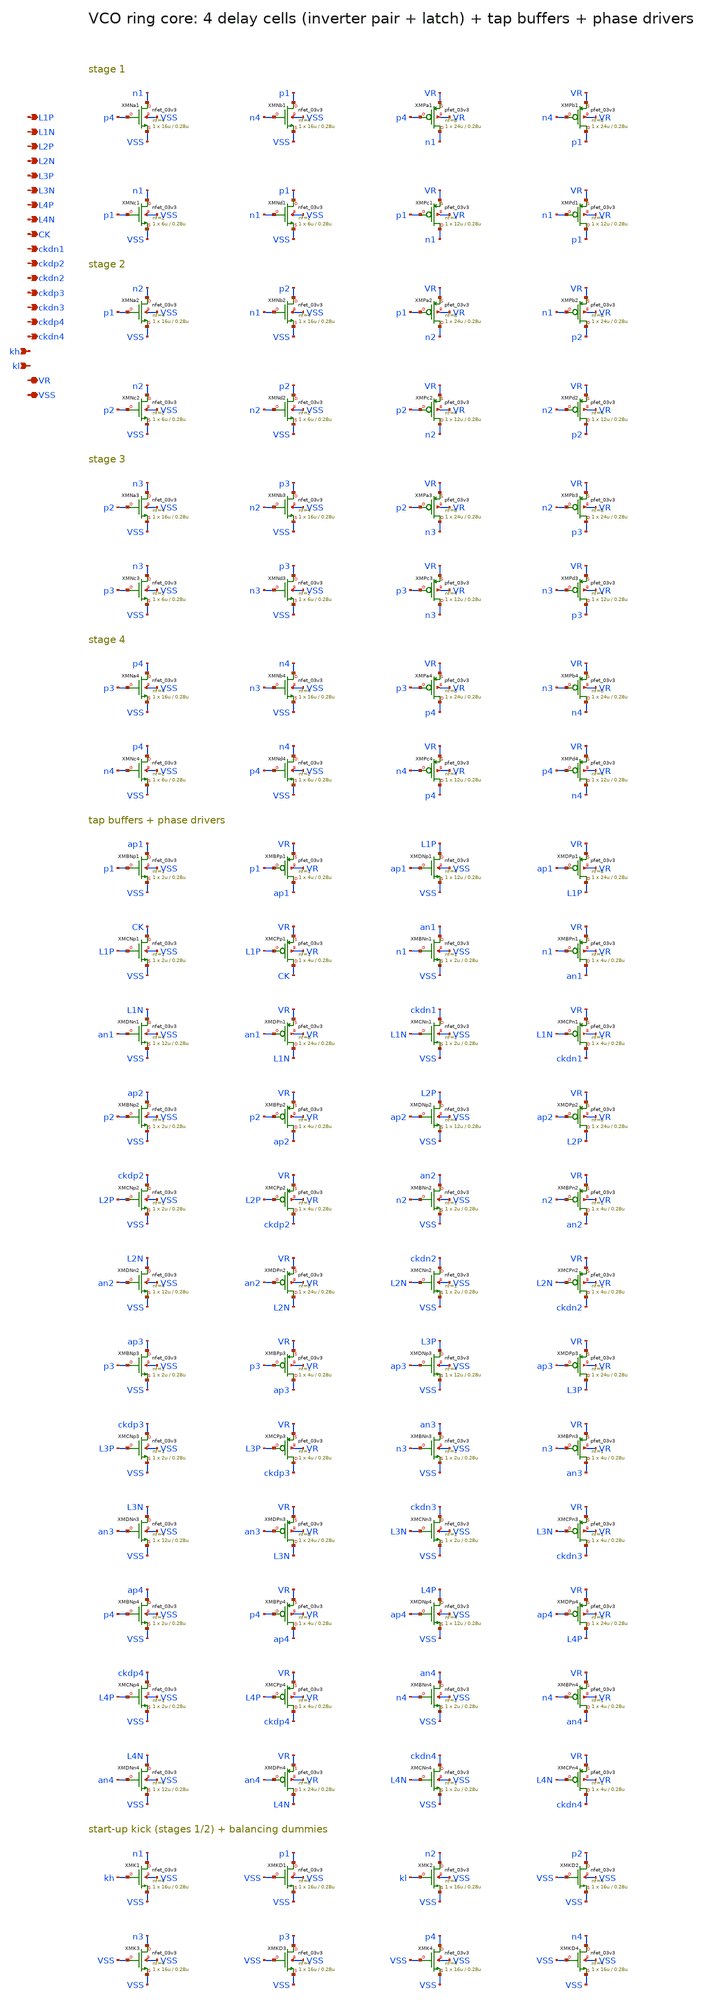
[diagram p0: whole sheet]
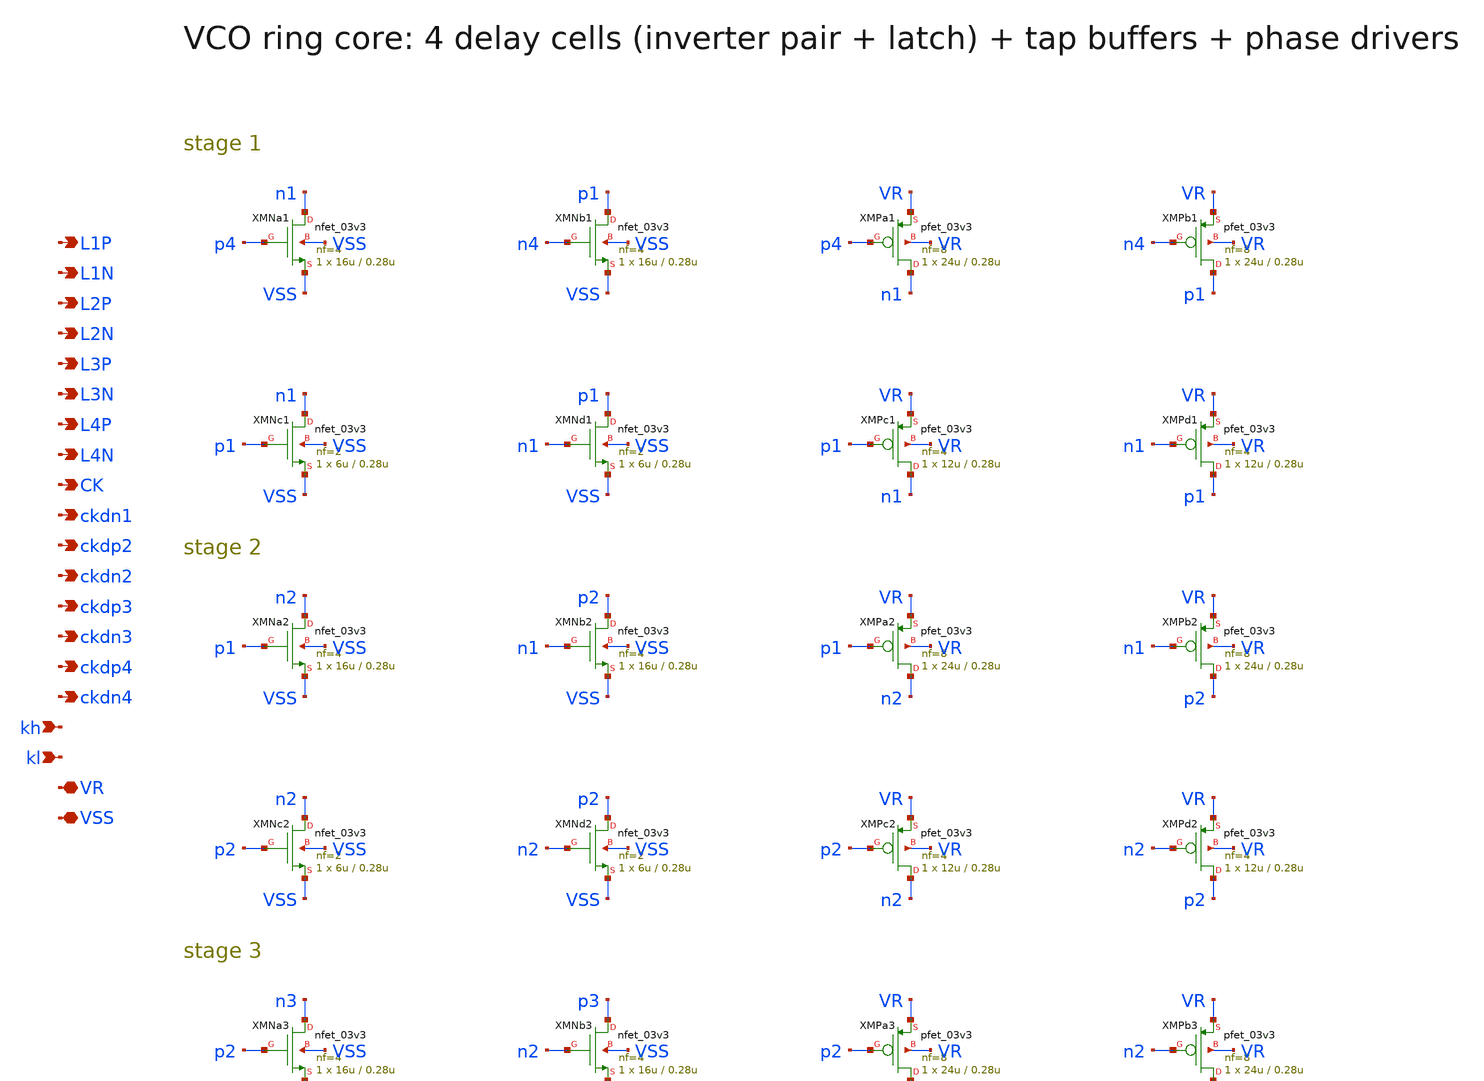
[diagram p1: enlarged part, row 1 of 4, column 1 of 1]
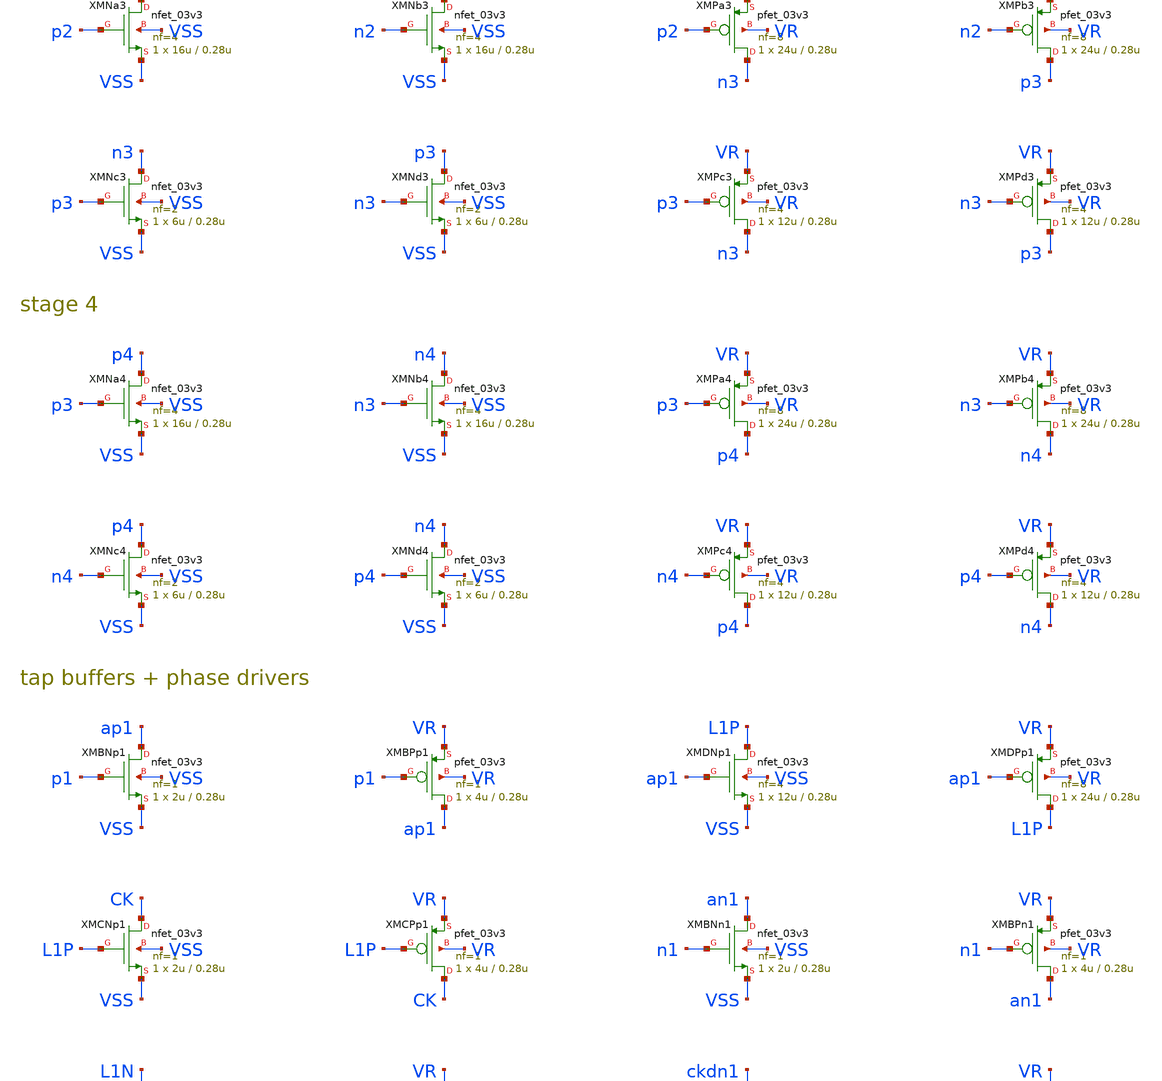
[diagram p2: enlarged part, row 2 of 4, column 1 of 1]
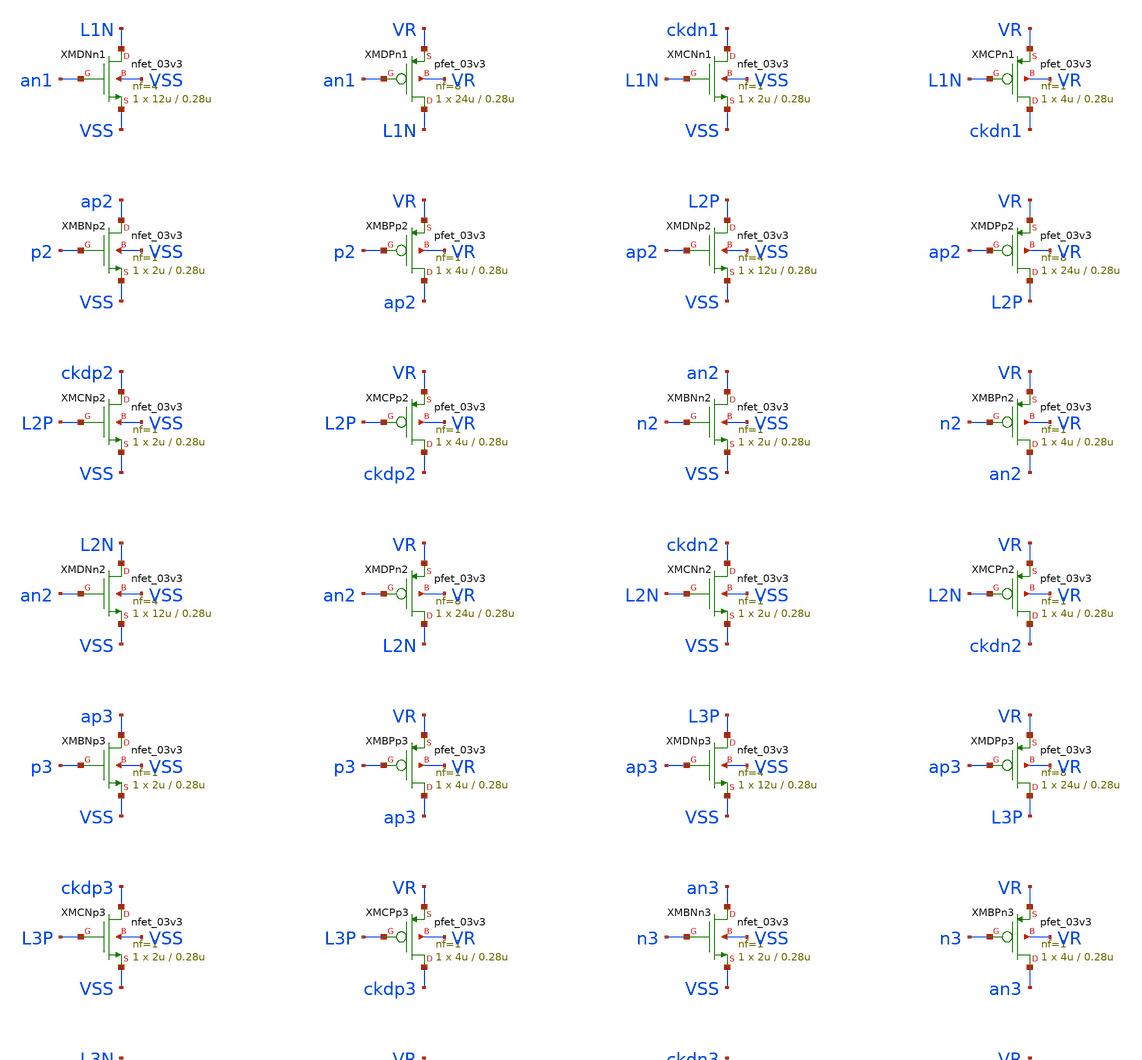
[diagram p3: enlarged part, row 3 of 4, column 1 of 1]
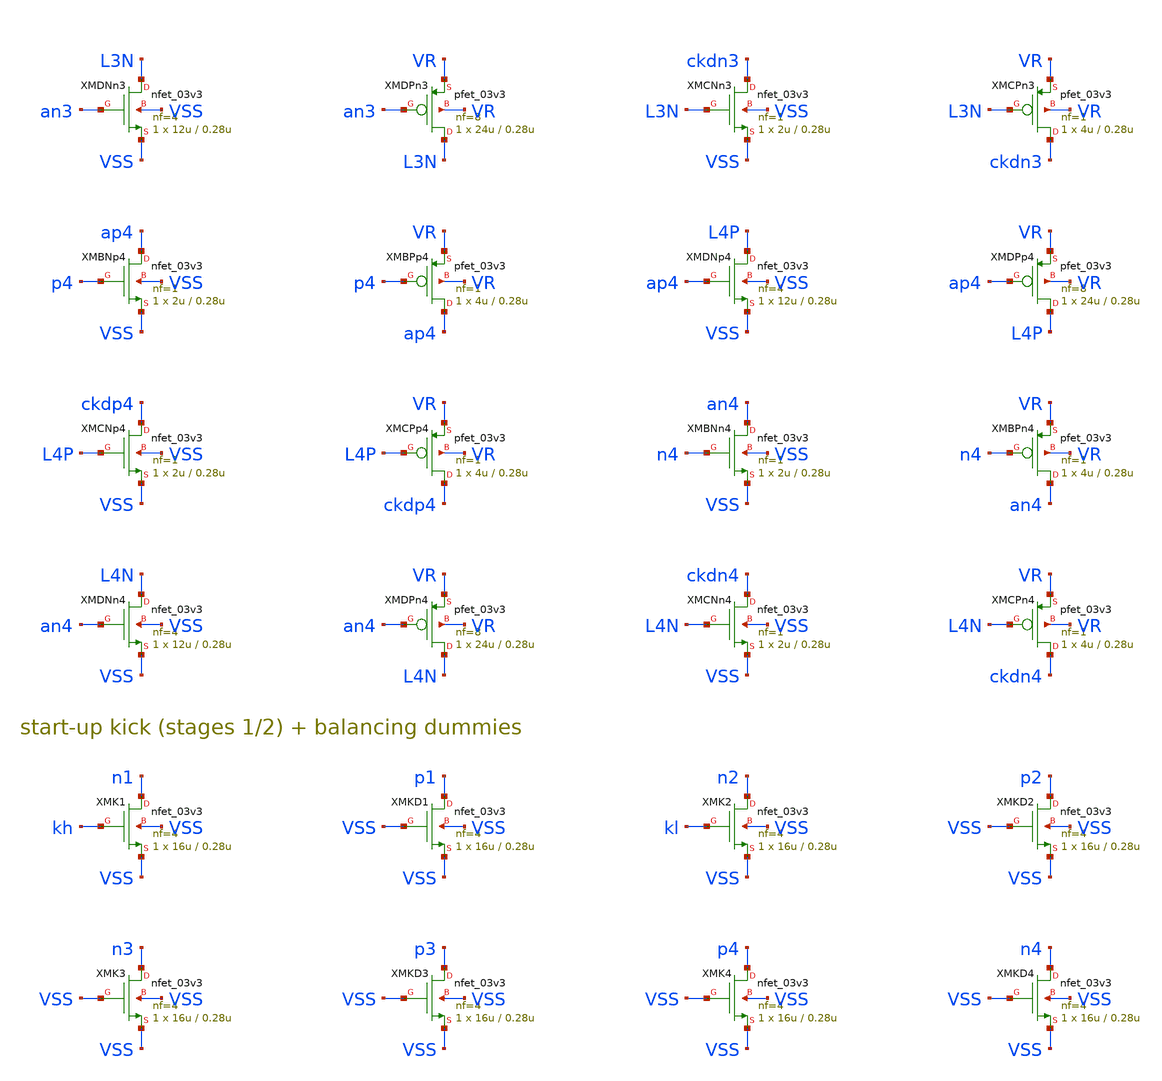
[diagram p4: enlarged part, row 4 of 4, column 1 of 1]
** sch_path: v1_claude/xschem/vco_core.sch
**.subckt vco_core L1P L1N L2P L2N L3P L3N L4P L4N CK ckdn1 ckdp2 ckdn2 ckdp3 ckdn3 ckdp4 ckdn4 kh
*+ kl VR VSS
*.opin L1P
*.opin L1N
*.opin L2P
*.opin L2N
*.opin L3P
*.opin L3N
*.opin L4P
*.opin L4N
*.opin CK
*.opin ckdn1
*.opin ckdp2
*.opin ckdn2
*.opin ckdp3
*.opin ckdn3
*.opin ckdp4
*.opin ckdn4
*.ipin kh
*.ipin kl
*.iopin VR
*.iopin VSS
XMNa1 n1 p4 VSS VSS nfet_03v3 L=0.28u W=16u nf=4 ad='int((nf+1)/2) * W/nf * 0.18u' as='int((nf+2)/2) * W/nf * 0.18u'
+ pd='2*int((nf+1)/2) * (W/nf + 0.18u)' ps='2*int((nf+2)/2) * (W/nf + 0.18u)' nrd='0.18u / W' nrs='0.18u / W'
+ sa=0 sb=0 sd=0 m=1
XMNb1 p1 n4 VSS VSS nfet_03v3 L=0.28u W=16u nf=4 ad='int((nf+1)/2) * W/nf * 0.18u' as='int((nf+2)/2) * W/nf * 0.18u'
+ pd='2*int((nf+1)/2) * (W/nf + 0.18u)' ps='2*int((nf+2)/2) * (W/nf + 0.18u)' nrd='0.18u / W' nrs='0.18u / W'
+ sa=0 sb=0 sd=0 m=1
XMPa1 n1 p4 VR VR pfet_03v3 L=0.28u W=24u nf=8 ad='int((nf+1)/2) * W/nf * 0.18u' as='int((nf+2)/2) * W/nf * 0.18u'
+ pd='2*int((nf+1)/2) * (W/nf + 0.18u)' ps='2*int((nf+2)/2) * (W/nf + 0.18u)' nrd='0.18u / W' nrs='0.18u / W'
+ sa=0 sb=0 sd=0 m=1
XMPb1 p1 n4 VR VR pfet_03v3 L=0.28u W=24u nf=8 ad='int((nf+1)/2) * W/nf * 0.18u' as='int((nf+2)/2) * W/nf * 0.18u'
+ pd='2*int((nf+1)/2) * (W/nf + 0.18u)' ps='2*int((nf+2)/2) * (W/nf + 0.18u)' nrd='0.18u / W' nrs='0.18u / W'
+ sa=0 sb=0 sd=0 m=1
XMNc1 n1 p1 VSS VSS nfet_03v3 L=0.28u W=6u nf=2 ad='int((nf+1)/2) * W/nf * 0.18u' as='int((nf+2)/2) * W/nf * 0.18u'
+ pd='2*int((nf+1)/2) * (W/nf + 0.18u)' ps='2*int((nf+2)/2) * (W/nf + 0.18u)' nrd='0.18u / W' nrs='0.18u / W'
+ sa=0 sb=0 sd=0 m=1
XMNd1 p1 n1 VSS VSS nfet_03v3 L=0.28u W=6u nf=2 ad='int((nf+1)/2) * W/nf * 0.18u' as='int((nf+2)/2) * W/nf * 0.18u'
+ pd='2*int((nf+1)/2) * (W/nf + 0.18u)' ps='2*int((nf+2)/2) * (W/nf + 0.18u)' nrd='0.18u / W' nrs='0.18u / W'
+ sa=0 sb=0 sd=0 m=1
XMPc1 n1 p1 VR VR pfet_03v3 L=0.28u W=12u nf=4 ad='int((nf+1)/2) * W/nf * 0.18u' as='int((nf+2)/2) * W/nf * 0.18u'
+ pd='2*int((nf+1)/2) * (W/nf + 0.18u)' ps='2*int((nf+2)/2) * (W/nf + 0.18u)' nrd='0.18u / W' nrs='0.18u / W'
+ sa=0 sb=0 sd=0 m=1
XMPd1 p1 n1 VR VR pfet_03v3 L=0.28u W=12u nf=4 ad='int((nf+1)/2) * W/nf * 0.18u' as='int((nf+2)/2) * W/nf * 0.18u'
+ pd='2*int((nf+1)/2) * (W/nf + 0.18u)' ps='2*int((nf+2)/2) * (W/nf + 0.18u)' nrd='0.18u / W' nrs='0.18u / W'
+ sa=0 sb=0 sd=0 m=1
XMNa2 n2 p1 VSS VSS nfet_03v3 L=0.28u W=16u nf=4 ad='int((nf+1)/2) * W/nf * 0.18u' as='int((nf+2)/2) * W/nf * 0.18u'
+ pd='2*int((nf+1)/2) * (W/nf + 0.18u)' ps='2*int((nf+2)/2) * (W/nf + 0.18u)' nrd='0.18u / W' nrs='0.18u / W'
+ sa=0 sb=0 sd=0 m=1
XMNb2 p2 n1 VSS VSS nfet_03v3 L=0.28u W=16u nf=4 ad='int((nf+1)/2) * W/nf * 0.18u' as='int((nf+2)/2) * W/nf * 0.18u'
+ pd='2*int((nf+1)/2) * (W/nf + 0.18u)' ps='2*int((nf+2)/2) * (W/nf + 0.18u)' nrd='0.18u / W' nrs='0.18u / W'
+ sa=0 sb=0 sd=0 m=1
XMPa2 n2 p1 VR VR pfet_03v3 L=0.28u W=24u nf=8 ad='int((nf+1)/2) * W/nf * 0.18u' as='int((nf+2)/2) * W/nf * 0.18u'
+ pd='2*int((nf+1)/2) * (W/nf + 0.18u)' ps='2*int((nf+2)/2) * (W/nf + 0.18u)' nrd='0.18u / W' nrs='0.18u / W'
+ sa=0 sb=0 sd=0 m=1
XMPb2 p2 n1 VR VR pfet_03v3 L=0.28u W=24u nf=8 ad='int((nf+1)/2) * W/nf * 0.18u' as='int((nf+2)/2) * W/nf * 0.18u'
+ pd='2*int((nf+1)/2) * (W/nf + 0.18u)' ps='2*int((nf+2)/2) * (W/nf + 0.18u)' nrd='0.18u / W' nrs='0.18u / W'
+ sa=0 sb=0 sd=0 m=1
XMNc2 n2 p2 VSS VSS nfet_03v3 L=0.28u W=6u nf=2 ad='int((nf+1)/2) * W/nf * 0.18u' as='int((nf+2)/2) * W/nf * 0.18u'
+ pd='2*int((nf+1)/2) * (W/nf + 0.18u)' ps='2*int((nf+2)/2) * (W/nf + 0.18u)' nrd='0.18u / W' nrs='0.18u / W'
+ sa=0 sb=0 sd=0 m=1
XMNd2 p2 n2 VSS VSS nfet_03v3 L=0.28u W=6u nf=2 ad='int((nf+1)/2) * W/nf * 0.18u' as='int((nf+2)/2) * W/nf * 0.18u'
+ pd='2*int((nf+1)/2) * (W/nf + 0.18u)' ps='2*int((nf+2)/2) * (W/nf + 0.18u)' nrd='0.18u / W' nrs='0.18u / W'
+ sa=0 sb=0 sd=0 m=1
XMPc2 n2 p2 VR VR pfet_03v3 L=0.28u W=12u nf=4 ad='int((nf+1)/2) * W/nf * 0.18u' as='int((nf+2)/2) * W/nf * 0.18u'
+ pd='2*int((nf+1)/2) * (W/nf + 0.18u)' ps='2*int((nf+2)/2) * (W/nf + 0.18u)' nrd='0.18u / W' nrs='0.18u / W'
+ sa=0 sb=0 sd=0 m=1
XMPd2 p2 n2 VR VR pfet_03v3 L=0.28u W=12u nf=4 ad='int((nf+1)/2) * W/nf * 0.18u' as='int((nf+2)/2) * W/nf * 0.18u'
+ pd='2*int((nf+1)/2) * (W/nf + 0.18u)' ps='2*int((nf+2)/2) * (W/nf + 0.18u)' nrd='0.18u / W' nrs='0.18u / W'
+ sa=0 sb=0 sd=0 m=1
XMNa3 n3 p2 VSS VSS nfet_03v3 L=0.28u W=16u nf=4 ad='int((nf+1)/2) * W/nf * 0.18u' as='int((nf+2)/2) * W/nf * 0.18u'
+ pd='2*int((nf+1)/2) * (W/nf + 0.18u)' ps='2*int((nf+2)/2) * (W/nf + 0.18u)' nrd='0.18u / W' nrs='0.18u / W'
+ sa=0 sb=0 sd=0 m=1
XMNb3 p3 n2 VSS VSS nfet_03v3 L=0.28u W=16u nf=4 ad='int((nf+1)/2) * W/nf * 0.18u' as='int((nf+2)/2) * W/nf * 0.18u'
+ pd='2*int((nf+1)/2) * (W/nf + 0.18u)' ps='2*int((nf+2)/2) * (W/nf + 0.18u)' nrd='0.18u / W' nrs='0.18u / W'
+ sa=0 sb=0 sd=0 m=1
XMPa3 n3 p2 VR VR pfet_03v3 L=0.28u W=24u nf=8 ad='int((nf+1)/2) * W/nf * 0.18u' as='int((nf+2)/2) * W/nf * 0.18u'
+ pd='2*int((nf+1)/2) * (W/nf + 0.18u)' ps='2*int((nf+2)/2) * (W/nf + 0.18u)' nrd='0.18u / W' nrs='0.18u / W'
+ sa=0 sb=0 sd=0 m=1
XMPb3 p3 n2 VR VR pfet_03v3 L=0.28u W=24u nf=8 ad='int((nf+1)/2) * W/nf * 0.18u' as='int((nf+2)/2) * W/nf * 0.18u'
+ pd='2*int((nf+1)/2) * (W/nf + 0.18u)' ps='2*int((nf+2)/2) * (W/nf + 0.18u)' nrd='0.18u / W' nrs='0.18u / W'
+ sa=0 sb=0 sd=0 m=1
XMNc3 n3 p3 VSS VSS nfet_03v3 L=0.28u W=6u nf=2 ad='int((nf+1)/2) * W/nf * 0.18u' as='int((nf+2)/2) * W/nf * 0.18u'
+ pd='2*int((nf+1)/2) * (W/nf + 0.18u)' ps='2*int((nf+2)/2) * (W/nf + 0.18u)' nrd='0.18u / W' nrs='0.18u / W'
+ sa=0 sb=0 sd=0 m=1
XMNd3 p3 n3 VSS VSS nfet_03v3 L=0.28u W=6u nf=2 ad='int((nf+1)/2) * W/nf * 0.18u' as='int((nf+2)/2) * W/nf * 0.18u'
+ pd='2*int((nf+1)/2) * (W/nf + 0.18u)' ps='2*int((nf+2)/2) * (W/nf + 0.18u)' nrd='0.18u / W' nrs='0.18u / W'
+ sa=0 sb=0 sd=0 m=1
XMPc3 n3 p3 VR VR pfet_03v3 L=0.28u W=12u nf=4 ad='int((nf+1)/2) * W/nf * 0.18u' as='int((nf+2)/2) * W/nf * 0.18u'
+ pd='2*int((nf+1)/2) * (W/nf + 0.18u)' ps='2*int((nf+2)/2) * (W/nf + 0.18u)' nrd='0.18u / W' nrs='0.18u / W'
+ sa=0 sb=0 sd=0 m=1
XMPd3 p3 n3 VR VR pfet_03v3 L=0.28u W=12u nf=4 ad='int((nf+1)/2) * W/nf * 0.18u' as='int((nf+2)/2) * W/nf * 0.18u'
+ pd='2*int((nf+1)/2) * (W/nf + 0.18u)' ps='2*int((nf+2)/2) * (W/nf + 0.18u)' nrd='0.18u / W' nrs='0.18u / W'
+ sa=0 sb=0 sd=0 m=1
XMNa4 p4 p3 VSS VSS nfet_03v3 L=0.28u W=16u nf=4 ad='int((nf+1)/2) * W/nf * 0.18u' as='int((nf+2)/2) * W/nf * 0.18u'
+ pd='2*int((nf+1)/2) * (W/nf + 0.18u)' ps='2*int((nf+2)/2) * (W/nf + 0.18u)' nrd='0.18u / W' nrs='0.18u / W'
+ sa=0 sb=0 sd=0 m=1
XMNb4 n4 n3 VSS VSS nfet_03v3 L=0.28u W=16u nf=4 ad='int((nf+1)/2) * W/nf * 0.18u' as='int((nf+2)/2) * W/nf * 0.18u'
+ pd='2*int((nf+1)/2) * (W/nf + 0.18u)' ps='2*int((nf+2)/2) * (W/nf + 0.18u)' nrd='0.18u / W' nrs='0.18u / W'
+ sa=0 sb=0 sd=0 m=1
XMPa4 p4 p3 VR VR pfet_03v3 L=0.28u W=24u nf=8 ad='int((nf+1)/2) * W/nf * 0.18u' as='int((nf+2)/2) * W/nf * 0.18u'
+ pd='2*int((nf+1)/2) * (W/nf + 0.18u)' ps='2*int((nf+2)/2) * (W/nf + 0.18u)' nrd='0.18u / W' nrs='0.18u / W'
+ sa=0 sb=0 sd=0 m=1
XMPb4 n4 n3 VR VR pfet_03v3 L=0.28u W=24u nf=8 ad='int((nf+1)/2) * W/nf * 0.18u' as='int((nf+2)/2) * W/nf * 0.18u'
+ pd='2*int((nf+1)/2) * (W/nf + 0.18u)' ps='2*int((nf+2)/2) * (W/nf + 0.18u)' nrd='0.18u / W' nrs='0.18u / W'
+ sa=0 sb=0 sd=0 m=1
XMNc4 p4 n4 VSS VSS nfet_03v3 L=0.28u W=6u nf=2 ad='int((nf+1)/2) * W/nf * 0.18u' as='int((nf+2)/2) * W/nf * 0.18u'
+ pd='2*int((nf+1)/2) * (W/nf + 0.18u)' ps='2*int((nf+2)/2) * (W/nf + 0.18u)' nrd='0.18u / W' nrs='0.18u / W'
+ sa=0 sb=0 sd=0 m=1
XMNd4 n4 p4 VSS VSS nfet_03v3 L=0.28u W=6u nf=2 ad='int((nf+1)/2) * W/nf * 0.18u' as='int((nf+2)/2) * W/nf * 0.18u'
+ pd='2*int((nf+1)/2) * (W/nf + 0.18u)' ps='2*int((nf+2)/2) * (W/nf + 0.18u)' nrd='0.18u / W' nrs='0.18u / W'
+ sa=0 sb=0 sd=0 m=1
XMPc4 p4 n4 VR VR pfet_03v3 L=0.28u W=12u nf=4 ad='int((nf+1)/2) * W/nf * 0.18u' as='int((nf+2)/2) * W/nf * 0.18u'
+ pd='2*int((nf+1)/2) * (W/nf + 0.18u)' ps='2*int((nf+2)/2) * (W/nf + 0.18u)' nrd='0.18u / W' nrs='0.18u / W'
+ sa=0 sb=0 sd=0 m=1
XMPd4 n4 p4 VR VR pfet_03v3 L=0.28u W=12u nf=4 ad='int((nf+1)/2) * W/nf * 0.18u' as='int((nf+2)/2) * W/nf * 0.18u'
+ pd='2*int((nf+1)/2) * (W/nf + 0.18u)' ps='2*int((nf+2)/2) * (W/nf + 0.18u)' nrd='0.18u / W' nrs='0.18u / W'
+ sa=0 sb=0 sd=0 m=1
XMBNp1 ap1 p1 VSS VSS nfet_03v3 L=0.28u W=2u nf=1 ad='int((nf+1)/2) * W/nf * 0.18u' as='int((nf+2)/2) * W/nf * 0.18u'
+ pd='2*int((nf+1)/2) * (W/nf + 0.18u)' ps='2*int((nf+2)/2) * (W/nf + 0.18u)' nrd='0.18u / W' nrs='0.18u / W'
+ sa=0 sb=0 sd=0 m=1
XMBPp1 ap1 p1 VR VR pfet_03v3 L=0.28u W=4u nf=1 ad='int((nf+1)/2) * W/nf * 0.18u' as='int((nf+2)/2) * W/nf * 0.18u'
+ pd='2*int((nf+1)/2) * (W/nf + 0.18u)' ps='2*int((nf+2)/2) * (W/nf + 0.18u)' nrd='0.18u / W' nrs='0.18u / W'
+ sa=0 sb=0 sd=0 m=1
XMDNp1 L1P ap1 VSS VSS nfet_03v3 L=0.28u W=12u nf=4 ad='int((nf+1)/2) * W/nf * 0.18u' as='int((nf+2)/2) * W/nf * 0.18u'
+ pd='2*int((nf+1)/2) * (W/nf + 0.18u)' ps='2*int((nf+2)/2) * (W/nf + 0.18u)' nrd='0.18u / W' nrs='0.18u / W'
+ sa=0 sb=0 sd=0 m=1
XMDPp1 L1P ap1 VR VR pfet_03v3 L=0.28u W=24u nf=8 ad='int((nf+1)/2) * W/nf * 0.18u' as='int((nf+2)/2) * W/nf * 0.18u'
+ pd='2*int((nf+1)/2) * (W/nf + 0.18u)' ps='2*int((nf+2)/2) * (W/nf + 0.18u)' nrd='0.18u / W' nrs='0.18u / W'
+ sa=0 sb=0 sd=0 m=1
XMCNp1 CK L1P VSS VSS nfet_03v3 L=0.28u W=2u nf=1 ad='int((nf+1)/2) * W/nf * 0.18u' as='int((nf+2)/2) * W/nf * 0.18u'
+ pd='2*int((nf+1)/2) * (W/nf + 0.18u)' ps='2*int((nf+2)/2) * (W/nf + 0.18u)' nrd='0.18u / W' nrs='0.18u / W'
+ sa=0 sb=0 sd=0 m=1
XMCPp1 CK L1P VR VR pfet_03v3 L=0.28u W=4u nf=1 ad='int((nf+1)/2) * W/nf * 0.18u' as='int((nf+2)/2) * W/nf * 0.18u'
+ pd='2*int((nf+1)/2) * (W/nf + 0.18u)' ps='2*int((nf+2)/2) * (W/nf + 0.18u)' nrd='0.18u / W' nrs='0.18u / W'
+ sa=0 sb=0 sd=0 m=1
XMBNn1 an1 n1 VSS VSS nfet_03v3 L=0.28u W=2u nf=1 ad='int((nf+1)/2) * W/nf * 0.18u' as='int((nf+2)/2) * W/nf * 0.18u'
+ pd='2*int((nf+1)/2) * (W/nf + 0.18u)' ps='2*int((nf+2)/2) * (W/nf + 0.18u)' nrd='0.18u / W' nrs='0.18u / W'
+ sa=0 sb=0 sd=0 m=1
XMBPn1 an1 n1 VR VR pfet_03v3 L=0.28u W=4u nf=1 ad='int((nf+1)/2) * W/nf * 0.18u' as='int((nf+2)/2) * W/nf * 0.18u'
+ pd='2*int((nf+1)/2) * (W/nf + 0.18u)' ps='2*int((nf+2)/2) * (W/nf + 0.18u)' nrd='0.18u / W' nrs='0.18u / W'
+ sa=0 sb=0 sd=0 m=1
XMDNn1 L1N an1 VSS VSS nfet_03v3 L=0.28u W=12u nf=4 ad='int((nf+1)/2) * W/nf * 0.18u' as='int((nf+2)/2) * W/nf * 0.18u'
+ pd='2*int((nf+1)/2) * (W/nf + 0.18u)' ps='2*int((nf+2)/2) * (W/nf + 0.18u)' nrd='0.18u / W' nrs='0.18u / W'
+ sa=0 sb=0 sd=0 m=1
XMDPn1 L1N an1 VR VR pfet_03v3 L=0.28u W=24u nf=8 ad='int((nf+1)/2) * W/nf * 0.18u' as='int((nf+2)/2) * W/nf * 0.18u'
+ pd='2*int((nf+1)/2) * (W/nf + 0.18u)' ps='2*int((nf+2)/2) * (W/nf + 0.18u)' nrd='0.18u / W' nrs='0.18u / W'
+ sa=0 sb=0 sd=0 m=1
XMCNn1 ckdn1 L1N VSS VSS nfet_03v3 L=0.28u W=2u nf=1 ad='int((nf+1)/2) * W/nf * 0.18u' as='int((nf+2)/2) * W/nf * 0.18u'
+ pd='2*int((nf+1)/2) * (W/nf + 0.18u)' ps='2*int((nf+2)/2) * (W/nf + 0.18u)' nrd='0.18u / W' nrs='0.18u / W'
+ sa=0 sb=0 sd=0 m=1
XMCPn1 ckdn1 L1N VR VR pfet_03v3 L=0.28u W=4u nf=1 ad='int((nf+1)/2) * W/nf * 0.18u' as='int((nf+2)/2) * W/nf * 0.18u'
+ pd='2*int((nf+1)/2) * (W/nf + 0.18u)' ps='2*int((nf+2)/2) * (W/nf + 0.18u)' nrd='0.18u / W' nrs='0.18u / W'
+ sa=0 sb=0 sd=0 m=1
XMBNp2 ap2 p2 VSS VSS nfet_03v3 L=0.28u W=2u nf=1 ad='int((nf+1)/2) * W/nf * 0.18u' as='int((nf+2)/2) * W/nf * 0.18u'
+ pd='2*int((nf+1)/2) * (W/nf + 0.18u)' ps='2*int((nf+2)/2) * (W/nf + 0.18u)' nrd='0.18u / W' nrs='0.18u / W'
+ sa=0 sb=0 sd=0 m=1
XMBPp2 ap2 p2 VR VR pfet_03v3 L=0.28u W=4u nf=1 ad='int((nf+1)/2) * W/nf * 0.18u' as='int((nf+2)/2) * W/nf * 0.18u'
+ pd='2*int((nf+1)/2) * (W/nf + 0.18u)' ps='2*int((nf+2)/2) * (W/nf + 0.18u)' nrd='0.18u / W' nrs='0.18u / W'
+ sa=0 sb=0 sd=0 m=1
XMDNp2 L2P ap2 VSS VSS nfet_03v3 L=0.28u W=12u nf=4 ad='int((nf+1)/2) * W/nf * 0.18u' as='int((nf+2)/2) * W/nf * 0.18u'
+ pd='2*int((nf+1)/2) * (W/nf + 0.18u)' ps='2*int((nf+2)/2) * (W/nf + 0.18u)' nrd='0.18u / W' nrs='0.18u / W'
+ sa=0 sb=0 sd=0 m=1
XMDPp2 L2P ap2 VR VR pfet_03v3 L=0.28u W=24u nf=8 ad='int((nf+1)/2) * W/nf * 0.18u' as='int((nf+2)/2) * W/nf * 0.18u'
+ pd='2*int((nf+1)/2) * (W/nf + 0.18u)' ps='2*int((nf+2)/2) * (W/nf + 0.18u)' nrd='0.18u / W' nrs='0.18u / W'
+ sa=0 sb=0 sd=0 m=1
XMCNp2 ckdp2 L2P VSS VSS nfet_03v3 L=0.28u W=2u nf=1 ad='int((nf+1)/2) * W/nf * 0.18u' as='int((nf+2)/2) * W/nf * 0.18u'
+ pd='2*int((nf+1)/2) * (W/nf + 0.18u)' ps='2*int((nf+2)/2) * (W/nf + 0.18u)' nrd='0.18u / W' nrs='0.18u / W'
+ sa=0 sb=0 sd=0 m=1
XMCPp2 ckdp2 L2P VR VR pfet_03v3 L=0.28u W=4u nf=1 ad='int((nf+1)/2) * W/nf * 0.18u' as='int((nf+2)/2) * W/nf * 0.18u'
+ pd='2*int((nf+1)/2) * (W/nf + 0.18u)' ps='2*int((nf+2)/2) * (W/nf + 0.18u)' nrd='0.18u / W' nrs='0.18u / W'
+ sa=0 sb=0 sd=0 m=1
XMBNn2 an2 n2 VSS VSS nfet_03v3 L=0.28u W=2u nf=1 ad='int((nf+1)/2) * W/nf * 0.18u' as='int((nf+2)/2) * W/nf * 0.18u'
+ pd='2*int((nf+1)/2) * (W/nf + 0.18u)' ps='2*int((nf+2)/2) * (W/nf + 0.18u)' nrd='0.18u / W' nrs='0.18u / W'
+ sa=0 sb=0 sd=0 m=1
XMBPn2 an2 n2 VR VR pfet_03v3 L=0.28u W=4u nf=1 ad='int((nf+1)/2) * W/nf * 0.18u' as='int((nf+2)/2) * W/nf * 0.18u'
+ pd='2*int((nf+1)/2) * (W/nf + 0.18u)' ps='2*int((nf+2)/2) * (W/nf + 0.18u)' nrd='0.18u / W' nrs='0.18u / W'
+ sa=0 sb=0 sd=0 m=1
XMDNn2 L2N an2 VSS VSS nfet_03v3 L=0.28u W=12u nf=4 ad='int((nf+1)/2) * W/nf * 0.18u' as='int((nf+2)/2) * W/nf * 0.18u'
+ pd='2*int((nf+1)/2) * (W/nf + 0.18u)' ps='2*int((nf+2)/2) * (W/nf + 0.18u)' nrd='0.18u / W' nrs='0.18u / W'
+ sa=0 sb=0 sd=0 m=1
XMDPn2 L2N an2 VR VR pfet_03v3 L=0.28u W=24u nf=8 ad='int((nf+1)/2) * W/nf * 0.18u' as='int((nf+2)/2) * W/nf * 0.18u'
+ pd='2*int((nf+1)/2) * (W/nf + 0.18u)' ps='2*int((nf+2)/2) * (W/nf + 0.18u)' nrd='0.18u / W' nrs='0.18u / W'
+ sa=0 sb=0 sd=0 m=1
XMCNn2 ckdn2 L2N VSS VSS nfet_03v3 L=0.28u W=2u nf=1 ad='int((nf+1)/2) * W/nf * 0.18u' as='int((nf+2)/2) * W/nf * 0.18u'
+ pd='2*int((nf+1)/2) * (W/nf + 0.18u)' ps='2*int((nf+2)/2) * (W/nf + 0.18u)' nrd='0.18u / W' nrs='0.18u / W'
+ sa=0 sb=0 sd=0 m=1
XMCPn2 ckdn2 L2N VR VR pfet_03v3 L=0.28u W=4u nf=1 ad='int((nf+1)/2) * W/nf * 0.18u' as='int((nf+2)/2) * W/nf * 0.18u'
+ pd='2*int((nf+1)/2) * (W/nf + 0.18u)' ps='2*int((nf+2)/2) * (W/nf + 0.18u)' nrd='0.18u / W' nrs='0.18u / W'
+ sa=0 sb=0 sd=0 m=1
XMBNp3 ap3 p3 VSS VSS nfet_03v3 L=0.28u W=2u nf=1 ad='int((nf+1)/2) * W/nf * 0.18u' as='int((nf+2)/2) * W/nf * 0.18u'
+ pd='2*int((nf+1)/2) * (W/nf + 0.18u)' ps='2*int((nf+2)/2) * (W/nf + 0.18u)' nrd='0.18u / W' nrs='0.18u / W'
+ sa=0 sb=0 sd=0 m=1
XMBPp3 ap3 p3 VR VR pfet_03v3 L=0.28u W=4u nf=1 ad='int((nf+1)/2) * W/nf * 0.18u' as='int((nf+2)/2) * W/nf * 0.18u'
+ pd='2*int((nf+1)/2) * (W/nf + 0.18u)' ps='2*int((nf+2)/2) * (W/nf + 0.18u)' nrd='0.18u / W' nrs='0.18u / W'
+ sa=0 sb=0 sd=0 m=1
XMDNp3 L3P ap3 VSS VSS nfet_03v3 L=0.28u W=12u nf=4 ad='int((nf+1)/2) * W/nf * 0.18u' as='int((nf+2)/2) * W/nf * 0.18u'
+ pd='2*int((nf+1)/2) * (W/nf + 0.18u)' ps='2*int((nf+2)/2) * (W/nf + 0.18u)' nrd='0.18u / W' nrs='0.18u / W'
+ sa=0 sb=0 sd=0 m=1
XMDPp3 L3P ap3 VR VR pfet_03v3 L=0.28u W=24u nf=8 ad='int((nf+1)/2) * W/nf * 0.18u' as='int((nf+2)/2) * W/nf * 0.18u'
+ pd='2*int((nf+1)/2) * (W/nf + 0.18u)' ps='2*int((nf+2)/2) * (W/nf + 0.18u)' nrd='0.18u / W' nrs='0.18u / W'
+ sa=0 sb=0 sd=0 m=1
XMCNp3 ckdp3 L3P VSS VSS nfet_03v3 L=0.28u W=2u nf=1 ad='int((nf+1)/2) * W/nf * 0.18u' as='int((nf+2)/2) * W/nf * 0.18u'
+ pd='2*int((nf+1)/2) * (W/nf + 0.18u)' ps='2*int((nf+2)/2) * (W/nf + 0.18u)' nrd='0.18u / W' nrs='0.18u / W'
+ sa=0 sb=0 sd=0 m=1
XMCPp3 ckdp3 L3P VR VR pfet_03v3 L=0.28u W=4u nf=1 ad='int((nf+1)/2) * W/nf * 0.18u' as='int((nf+2)/2) * W/nf * 0.18u'
+ pd='2*int((nf+1)/2) * (W/nf + 0.18u)' ps='2*int((nf+2)/2) * (W/nf + 0.18u)' nrd='0.18u / W' nrs='0.18u / W'
+ sa=0 sb=0 sd=0 m=1
XMBNn3 an3 n3 VSS VSS nfet_03v3 L=0.28u W=2u nf=1 ad='int((nf+1)/2) * W/nf * 0.18u' as='int((nf+2)/2) * W/nf * 0.18u'
+ pd='2*int((nf+1)/2) * (W/nf + 0.18u)' ps='2*int((nf+2)/2) * (W/nf + 0.18u)' nrd='0.18u / W' nrs='0.18u / W'
+ sa=0 sb=0 sd=0 m=1
XMBPn3 an3 n3 VR VR pfet_03v3 L=0.28u W=4u nf=1 ad='int((nf+1)/2) * W/nf * 0.18u' as='int((nf+2)/2) * W/nf * 0.18u'
+ pd='2*int((nf+1)/2) * (W/nf + 0.18u)' ps='2*int((nf+2)/2) * (W/nf + 0.18u)' nrd='0.18u / W' nrs='0.18u / W'
+ sa=0 sb=0 sd=0 m=1
XMDNn3 L3N an3 VSS VSS nfet_03v3 L=0.28u W=12u nf=4 ad='int((nf+1)/2) * W/nf * 0.18u' as='int((nf+2)/2) * W/nf * 0.18u'
+ pd='2*int((nf+1)/2) * (W/nf + 0.18u)' ps='2*int((nf+2)/2) * (W/nf + 0.18u)' nrd='0.18u / W' nrs='0.18u / W'
+ sa=0 sb=0 sd=0 m=1
XMDPn3 L3N an3 VR VR pfet_03v3 L=0.28u W=24u nf=8 ad='int((nf+1)/2) * W/nf * 0.18u' as='int((nf+2)/2) * W/nf * 0.18u'
+ pd='2*int((nf+1)/2) * (W/nf + 0.18u)' ps='2*int((nf+2)/2) * (W/nf + 0.18u)' nrd='0.18u / W' nrs='0.18u / W'
+ sa=0 sb=0 sd=0 m=1
XMCNn3 ckdn3 L3N VSS VSS nfet_03v3 L=0.28u W=2u nf=1 ad='int((nf+1)/2) * W/nf * 0.18u' as='int((nf+2)/2) * W/nf * 0.18u'
+ pd='2*int((nf+1)/2) * (W/nf + 0.18u)' ps='2*int((nf+2)/2) * (W/nf + 0.18u)' nrd='0.18u / W' nrs='0.18u / W'
+ sa=0 sb=0 sd=0 m=1
XMCPn3 ckdn3 L3N VR VR pfet_03v3 L=0.28u W=4u nf=1 ad='int((nf+1)/2) * W/nf * 0.18u' as='int((nf+2)/2) * W/nf * 0.18u'
+ pd='2*int((nf+1)/2) * (W/nf + 0.18u)' ps='2*int((nf+2)/2) * (W/nf + 0.18u)' nrd='0.18u / W' nrs='0.18u / W'
+ sa=0 sb=0 sd=0 m=1
XMBNp4 ap4 p4 VSS VSS nfet_03v3 L=0.28u W=2u nf=1 ad='int((nf+1)/2) * W/nf * 0.18u' as='int((nf+2)/2) * W/nf * 0.18u'
+ pd='2*int((nf+1)/2) * (W/nf + 0.18u)' ps='2*int((nf+2)/2) * (W/nf + 0.18u)' nrd='0.18u / W' nrs='0.18u / W'
+ sa=0 sb=0 sd=0 m=1
XMBPp4 ap4 p4 VR VR pfet_03v3 L=0.28u W=4u nf=1 ad='int((nf+1)/2) * W/nf * 0.18u' as='int((nf+2)/2) * W/nf * 0.18u'
+ pd='2*int((nf+1)/2) * (W/nf + 0.18u)' ps='2*int((nf+2)/2) * (W/nf + 0.18u)' nrd='0.18u / W' nrs='0.18u / W'
+ sa=0 sb=0 sd=0 m=1
XMDNp4 L4P ap4 VSS VSS nfet_03v3 L=0.28u W=12u nf=4 ad='int((nf+1)/2) * W/nf * 0.18u' as='int((nf+2)/2) * W/nf * 0.18u'
+ pd='2*int((nf+1)/2) * (W/nf + 0.18u)' ps='2*int((nf+2)/2) * (W/nf + 0.18u)' nrd='0.18u / W' nrs='0.18u / W'
+ sa=0 sb=0 sd=0 m=1
XMDPp4 L4P ap4 VR VR pfet_03v3 L=0.28u W=24u nf=8 ad='int((nf+1)/2) * W/nf * 0.18u' as='int((nf+2)/2) * W/nf * 0.18u'
+ pd='2*int((nf+1)/2) * (W/nf + 0.18u)' ps='2*int((nf+2)/2) * (W/nf + 0.18u)' nrd='0.18u / W' nrs='0.18u / W'
+ sa=0 sb=0 sd=0 m=1
XMCNp4 ckdp4 L4P VSS VSS nfet_03v3 L=0.28u W=2u nf=1 ad='int((nf+1)/2) * W/nf * 0.18u' as='int((nf+2)/2) * W/nf * 0.18u'
+ pd='2*int((nf+1)/2) * (W/nf + 0.18u)' ps='2*int((nf+2)/2) * (W/nf + 0.18u)' nrd='0.18u / W' nrs='0.18u / W'
+ sa=0 sb=0 sd=0 m=1
XMCPp4 ckdp4 L4P VR VR pfet_03v3 L=0.28u W=4u nf=1 ad='int((nf+1)/2) * W/nf * 0.18u' as='int((nf+2)/2) * W/nf * 0.18u'
+ pd='2*int((nf+1)/2) * (W/nf + 0.18u)' ps='2*int((nf+2)/2) * (W/nf + 0.18u)' nrd='0.18u / W' nrs='0.18u / W'
+ sa=0 sb=0 sd=0 m=1
XMBNn4 an4 n4 VSS VSS nfet_03v3 L=0.28u W=2u nf=1 ad='int((nf+1)/2) * W/nf * 0.18u' as='int((nf+2)/2) * W/nf * 0.18u'
+ pd='2*int((nf+1)/2) * (W/nf + 0.18u)' ps='2*int((nf+2)/2) * (W/nf + 0.18u)' nrd='0.18u / W' nrs='0.18u / W'
+ sa=0 sb=0 sd=0 m=1
XMBPn4 an4 n4 VR VR pfet_03v3 L=0.28u W=4u nf=1 ad='int((nf+1)/2) * W/nf * 0.18u' as='int((nf+2)/2) * W/nf * 0.18u'
+ pd='2*int((nf+1)/2) * (W/nf + 0.18u)' ps='2*int((nf+2)/2) * (W/nf + 0.18u)' nrd='0.18u / W' nrs='0.18u / W'
+ sa=0 sb=0 sd=0 m=1
XMDNn4 L4N an4 VSS VSS nfet_03v3 L=0.28u W=12u nf=4 ad='int((nf+1)/2) * W/nf * 0.18u' as='int((nf+2)/2) * W/nf * 0.18u'
+ pd='2*int((nf+1)/2) * (W/nf + 0.18u)' ps='2*int((nf+2)/2) * (W/nf + 0.18u)' nrd='0.18u / W' nrs='0.18u / W'
+ sa=0 sb=0 sd=0 m=1
XMDPn4 L4N an4 VR VR pfet_03v3 L=0.28u W=24u nf=8 ad='int((nf+1)/2) * W/nf * 0.18u' as='int((nf+2)/2) * W/nf * 0.18u'
+ pd='2*int((nf+1)/2) * (W/nf + 0.18u)' ps='2*int((nf+2)/2) * (W/nf + 0.18u)' nrd='0.18u / W' nrs='0.18u / W'
+ sa=0 sb=0 sd=0 m=1
XMCNn4 ckdn4 L4N VSS VSS nfet_03v3 L=0.28u W=2u nf=1 ad='int((nf+1)/2) * W/nf * 0.18u' as='int((nf+2)/2) * W/nf * 0.18u'
+ pd='2*int((nf+1)/2) * (W/nf + 0.18u)' ps='2*int((nf+2)/2) * (W/nf + 0.18u)' nrd='0.18u / W' nrs='0.18u / W'
+ sa=0 sb=0 sd=0 m=1
XMCPn4 ckdn4 L4N VR VR pfet_03v3 L=0.28u W=4u nf=1 ad='int((nf+1)/2) * W/nf * 0.18u' as='int((nf+2)/2) * W/nf * 0.18u'
+ pd='2*int((nf+1)/2) * (W/nf + 0.18u)' ps='2*int((nf+2)/2) * (W/nf + 0.18u)' nrd='0.18u / W' nrs='0.18u / W'
+ sa=0 sb=0 sd=0 m=1
XMK1 n1 kh VSS VSS nfet_03v3 L=0.28u W=16u nf=4 ad='int((nf+1)/2) * W/nf * 0.18u' as='int((nf+2)/2) * W/nf * 0.18u'
+ pd='2*int((nf+1)/2) * (W/nf + 0.18u)' ps='2*int((nf+2)/2) * (W/nf + 0.18u)' nrd='0.18u / W' nrs='0.18u / W'
+ sa=0 sb=0 sd=0 m=1
XMKD1 p1 VSS VSS VSS nfet_03v3 L=0.28u W=16u nf=4 ad='int((nf+1)/2) * W/nf * 0.18u' as='int((nf+2)/2) * W/nf * 0.18u'
+ pd='2*int((nf+1)/2) * (W/nf + 0.18u)' ps='2*int((nf+2)/2) * (W/nf + 0.18u)' nrd='0.18u / W' nrs='0.18u / W'
+ sa=0 sb=0 sd=0 m=1
XMK2 n2 kl VSS VSS nfet_03v3 L=0.28u W=16u nf=4 ad='int((nf+1)/2) * W/nf * 0.18u' as='int((nf+2)/2) * W/nf * 0.18u'
+ pd='2*int((nf+1)/2) * (W/nf + 0.18u)' ps='2*int((nf+2)/2) * (W/nf + 0.18u)' nrd='0.18u / W' nrs='0.18u / W'
+ sa=0 sb=0 sd=0 m=1
XMKD2 p2 VSS VSS VSS nfet_03v3 L=0.28u W=16u nf=4 ad='int((nf+1)/2) * W/nf * 0.18u' as='int((nf+2)/2) * W/nf * 0.18u'
+ pd='2*int((nf+1)/2) * (W/nf + 0.18u)' ps='2*int((nf+2)/2) * (W/nf + 0.18u)' nrd='0.18u / W' nrs='0.18u / W'
+ sa=0 sb=0 sd=0 m=1
XMK3 n3 VSS VSS VSS nfet_03v3 L=0.28u W=16u nf=4 ad='int((nf+1)/2) * W/nf * 0.18u' as='int((nf+2)/2) * W/nf * 0.18u'
+ pd='2*int((nf+1)/2) * (W/nf + 0.18u)' ps='2*int((nf+2)/2) * (W/nf + 0.18u)' nrd='0.18u / W' nrs='0.18u / W'
+ sa=0 sb=0 sd=0 m=1
XMKD3 p3 VSS VSS VSS nfet_03v3 L=0.28u W=16u nf=4 ad='int((nf+1)/2) * W/nf * 0.18u' as='int((nf+2)/2) * W/nf * 0.18u'
+ pd='2*int((nf+1)/2) * (W/nf + 0.18u)' ps='2*int((nf+2)/2) * (W/nf + 0.18u)' nrd='0.18u / W' nrs='0.18u / W'
+ sa=0 sb=0 sd=0 m=1
XMK4 p4 VSS VSS VSS nfet_03v3 L=0.28u W=16u nf=4 ad='int((nf+1)/2) * W/nf * 0.18u' as='int((nf+2)/2) * W/nf * 0.18u'
+ pd='2*int((nf+1)/2) * (W/nf + 0.18u)' ps='2*int((nf+2)/2) * (W/nf + 0.18u)' nrd='0.18u / W' nrs='0.18u / W'
+ sa=0 sb=0 sd=0 m=1
XMKD4 n4 VSS VSS VSS nfet_03v3 L=0.28u W=16u nf=4 ad='int((nf+1)/2) * W/nf * 0.18u' as='int((nf+2)/2) * W/nf * 0.18u'
+ pd='2*int((nf+1)/2) * (W/nf + 0.18u)' ps='2*int((nf+2)/2) * (W/nf + 0.18u)' nrd='0.18u / W' nrs='0.18u / W'
+ sa=0 sb=0 sd=0 m=1
**.ends
.end
